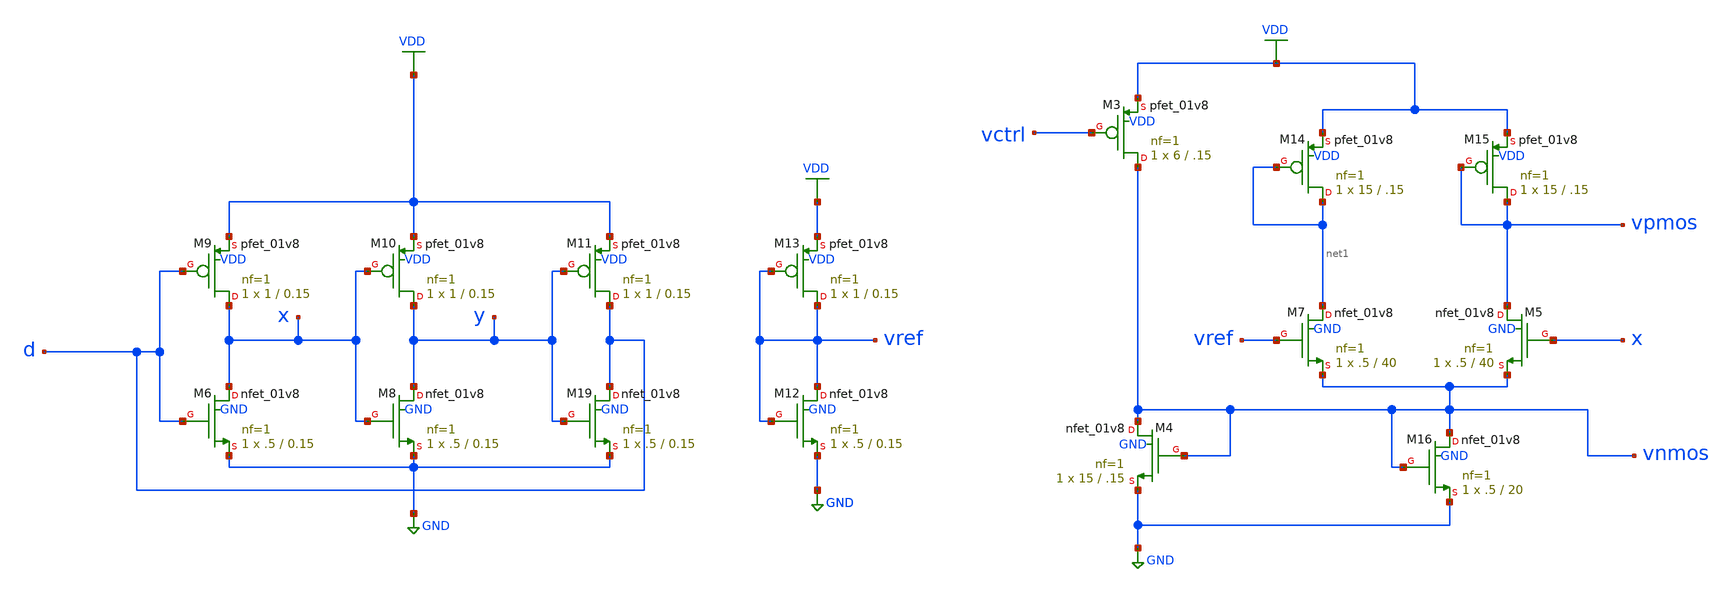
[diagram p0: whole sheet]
** sch_path: pll/ring_vco_lib/QRO_cell/xschem/aux_circuits.sch
**.subckt aux_circuits
XM6 x d GND GND sky130_fd_pr__nfet_01v8 L=0.15 W=.5 nf=1 ad='int((nf+1)/2) * W/nf * 0.29' as='int((nf+2)/2) * W/nf * 0.29'
+ pd='2*int((nf+1)/2) * (W/nf + 0.29)' ps='2*int((nf+2)/2) * (W/nf + 0.29)' nrd='0.29 / W' nrs='0.29 / W'
+ sa=0 sb=0 sd=0 mult=1 m=1
XM8 y x GND GND sky130_fd_pr__nfet_01v8 L=0.15 W=.5 nf=1 ad='int((nf+1)/2) * W/nf * 0.29' as='int((nf+2)/2) * W/nf * 0.29'
+ pd='2*int((nf+1)/2) * (W/nf + 0.29)' ps='2*int((nf+2)/2) * (W/nf + 0.29)' nrd='0.29 / W' nrs='0.29 / W'
+ sa=0 sb=0 sd=0 mult=1 m=1
XM19 d y GND GND sky130_fd_pr__nfet_01v8 L=0.15 W=.5 nf=1 ad='int((nf+1)/2) * W/nf * 0.29' as='int((nf+2)/2) * W/nf * 0.29'
+ pd='2*int((nf+1)/2) * (W/nf + 0.29)' ps='2*int((nf+2)/2) * (W/nf + 0.29)' nrd='0.29 / W' nrs='0.29 / W'
+ sa=0 sb=0 sd=0 mult=1 m=1
XM9 x d VDD VDD sky130_fd_pr__pfet_01v8 L=0.15 W=1 nf=1 ad='int((nf+1)/2) * W/nf * 0.29' as='int((nf+2)/2) * W/nf * 0.29'
+ pd='2*int((nf+1)/2) * (W/nf + 0.29)' ps='2*int((nf+2)/2) * (W/nf + 0.29)' nrd='0.29 / W' nrs='0.29 / W'
+ sa=0 sb=0 sd=0 mult=1 m=1
XM10 y x VDD VDD sky130_fd_pr__pfet_01v8 L=0.15 W=1 nf=1 ad='int((nf+1)/2) * W/nf * 0.29' as='int((nf+2)/2) * W/nf * 0.29'
+ pd='2*int((nf+1)/2) * (W/nf + 0.29)' ps='2*int((nf+2)/2) * (W/nf + 0.29)' nrd='0.29 / W' nrs='0.29 / W'
+ sa=0 sb=0 sd=0 mult=1 m=1
XM11 d y VDD VDD sky130_fd_pr__pfet_01v8 L=0.15 W=1 nf=1 ad='int((nf+1)/2) * W/nf * 0.29' as='int((nf+2)/2) * W/nf * 0.29'
+ pd='2*int((nf+1)/2) * (W/nf + 0.29)' ps='2*int((nf+2)/2) * (W/nf + 0.29)' nrd='0.29 / W' nrs='0.29 / W'
+ sa=0 sb=0 sd=0 mult=1 m=1
XM12 vref vref GND GND sky130_fd_pr__nfet_01v8 L=0.15 W=.5 nf=1 ad='int((nf+1)/2) * W/nf * 0.29' as='int((nf+2)/2) * W/nf * 0.29'
+ pd='2*int((nf+1)/2) * (W/nf + 0.29)' ps='2*int((nf+2)/2) * (W/nf + 0.29)' nrd='0.29 / W' nrs='0.29 / W'
+ sa=0 sb=0 sd=0 mult=1 m=1
XM13 vref vref VDD VDD sky130_fd_pr__pfet_01v8 L=0.15 W=1 nf=1 ad='int((nf+1)/2) * W/nf * 0.29' as='int((nf+2)/2) * W/nf * 0.29'
+ pd='2*int((nf+1)/2) * (W/nf + 0.29)' ps='2*int((nf+2)/2) * (W/nf + 0.29)' nrd='0.29 / W' nrs='0.29 / W'
+ sa=0 sb=0 sd=0 mult=1 m=1
XM16 vnmos vnmos GND GND sky130_fd_pr__nfet_01v8 L=20 W=.5 nf=1 ad='int((nf+1)/2) * W/nf * 0.29' as='int((nf+2)/2) * W/nf * 0.29'
+ pd='2*int((nf+1)/2) * (W/nf + 0.29)' ps='2*int((nf+2)/2) * (W/nf + 0.29)' nrd='0.29 / W' nrs='0.29 / W'
+ sa=0 sb=0 sd=0 mult=1 m=1
XM4 vnmos vnmos GND GND sky130_fd_pr__nfet_01v8 L=.15 W=15 nf=1 ad='int((nf+1)/2) * W/nf * 0.29' as='int((nf+2)/2) * W/nf * 0.29'
+ pd='2*int((nf+1)/2) * (W/nf + 0.29)' ps='2*int((nf+2)/2) * (W/nf + 0.29)' nrd='0.29 / W' nrs='0.29 / W'
+ sa=0 sb=0 sd=0 mult=1 m=1
XM5 vpmos x vnmos GND sky130_fd_pr__nfet_01v8 L=40 W=.5 nf=1 ad='int((nf+1)/2) * W/nf * 0.29' as='int((nf+2)/2) * W/nf * 0.29'
+ pd='2*int((nf+1)/2) * (W/nf + 0.29)' ps='2*int((nf+2)/2) * (W/nf + 0.29)' nrd='0.29 / W' nrs='0.29 / W'
+ sa=0 sb=0 sd=0 mult=1 m=1
XM7 net1 vref vnmos GND sky130_fd_pr__nfet_01v8 L=40 W=.5 nf=1 ad='int((nf+1)/2) * W/nf * 0.29' as='int((nf+2)/2) * W/nf * 0.29'
+ pd='2*int((nf+1)/2) * (W/nf + 0.29)' ps='2*int((nf+2)/2) * (W/nf + 0.29)' nrd='0.29 / W' nrs='0.29 / W'
+ sa=0 sb=0 sd=0 mult=1 m=1
XM14 net1 net1 VDD VDD sky130_fd_pr__pfet_01v8 L=.15 W=15 nf=1 ad='int((nf+1)/2) * W/nf * 0.29' as='int((nf+2)/2) * W/nf * 0.29'
+ pd='2*int((nf+1)/2) * (W/nf + 0.29)' ps='2*int((nf+2)/2) * (W/nf + 0.29)' nrd='0.29 / W' nrs='0.29 / W'
+ sa=0 sb=0 sd=0 mult=1 m=1
XM15 vpmos vpmos VDD VDD sky130_fd_pr__pfet_01v8 L=.15 W=15 nf=1 ad='int((nf+1)/2) * W/nf * 0.29' as='int((nf+2)/2) * W/nf * 0.29'
+ pd='2*int((nf+1)/2) * (W/nf + 0.29)' ps='2*int((nf+2)/2) * (W/nf + 0.29)' nrd='0.29 / W' nrs='0.29 / W'
+ sa=0 sb=0 sd=0 mult=1 m=1
XM3 vnmos vctrl VDD VDD sky130_fd_pr__pfet_01v8 L=.15 W=6 nf=1 ad='int((nf+1)/2) * W/nf * 0.29' as='int((nf+2)/2) * W/nf * 0.29'
+ pd='2*int((nf+1)/2) * (W/nf + 0.29)' ps='2*int((nf+2)/2) * (W/nf + 0.29)' nrd='0.29 / W' nrs='0.29 / W'
+ sa=0 sb=0 sd=0 mult=1 m=1
**.ends
.GLOBAL GND
.GLOBAL VDD
.end
